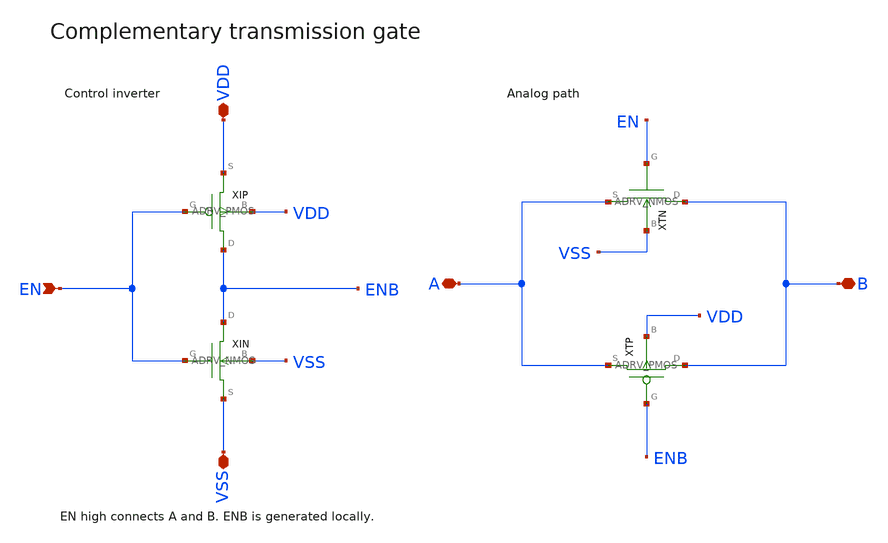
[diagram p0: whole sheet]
** sch_path: examples/sky130-programmable-gain/PGA_SWITCH.sch
**.subckt PGA_SWITCH EN VDD VSS A B
*.ipin EN
*.iopin VDD
*.iopin VSS
*.iopin A
*.iopin B
XIP ENB EN VDD VDD sky130_fd_pr__pfet_01v8 w=1.2 l=0.15 nf=1 ad=0.36 as=0.36 pd=3 ps=3 m=1
XIN ENB EN VSS VSS sky130_fd_pr__nfet_01v8 w=0.6 l=0.15 nf=1 ad=0.18 as=0.18 pd=1.8 ps=1.8 m=1
XTN B EN A VSS sky130_fd_pr__nfet_01v8 w=2 l=0.15 nf=1 ad=0.6 as=0.6 pd=4.6 ps=4.6 m=1
XTP B ENB A VDD sky130_fd_pr__pfet_01v8 w=4 l=0.15 nf=1 ad=1.2 as=1.2 pd=8.6 ps=8.6 m=1
**.ends
.end
